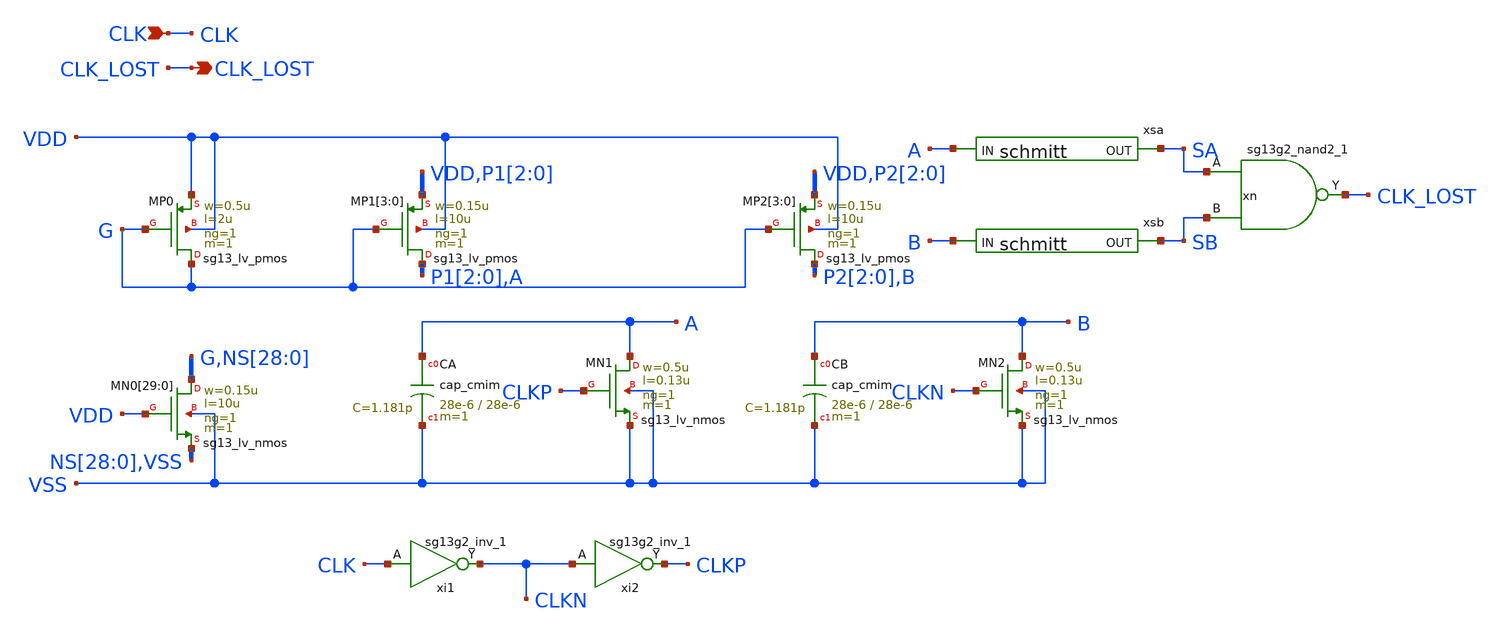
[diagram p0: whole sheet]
** sch_path: design/blocks/clkmon/schematic/wd_clkmon.sch
**.subckt wd_clkmon CLK CLK_LOST
*.ipin CLK
*.opin CLK_LOST
XMP0 G G VDD VDD sg13_lv_pmos w=0.5u l=2u ng=1 m=1 mm_ok=1
XMN0[29] G VDD NS[28] VSS sg13_lv_nmos w=0.15u l=10u ng=1 m=1 mm_ok=1
XMN0[28] NS[28] VDD NS[27] VSS sg13_lv_nmos w=0.15u l=10u ng=1 m=1 mm_ok=1
XMN0[27] NS[27] VDD NS[26] VSS sg13_lv_nmos w=0.15u l=10u ng=1 m=1 mm_ok=1
XMN0[26] NS[26] VDD NS[25] VSS sg13_lv_nmos w=0.15u l=10u ng=1 m=1 mm_ok=1
XMN0[25] NS[25] VDD NS[24] VSS sg13_lv_nmos w=0.15u l=10u ng=1 m=1 mm_ok=1
XMN0[24] NS[24] VDD NS[23] VSS sg13_lv_nmos w=0.15u l=10u ng=1 m=1 mm_ok=1
XMN0[23] NS[23] VDD NS[22] VSS sg13_lv_nmos w=0.15u l=10u ng=1 m=1 mm_ok=1
XMN0[22] NS[22] VDD NS[21] VSS sg13_lv_nmos w=0.15u l=10u ng=1 m=1 mm_ok=1
XMN0[21] NS[21] VDD NS[20] VSS sg13_lv_nmos w=0.15u l=10u ng=1 m=1 mm_ok=1
XMN0[20] NS[20] VDD NS[19] VSS sg13_lv_nmos w=0.15u l=10u ng=1 m=1 mm_ok=1
XMN0[19] NS[19] VDD NS[18] VSS sg13_lv_nmos w=0.15u l=10u ng=1 m=1 mm_ok=1
XMN0[18] NS[18] VDD NS[17] VSS sg13_lv_nmos w=0.15u l=10u ng=1 m=1 mm_ok=1
XMN0[17] NS[17] VDD NS[16] VSS sg13_lv_nmos w=0.15u l=10u ng=1 m=1 mm_ok=1
XMN0[16] NS[16] VDD NS[15] VSS sg13_lv_nmos w=0.15u l=10u ng=1 m=1 mm_ok=1
XMN0[15] NS[15] VDD NS[14] VSS sg13_lv_nmos w=0.15u l=10u ng=1 m=1 mm_ok=1
XMN0[14] NS[14] VDD NS[13] VSS sg13_lv_nmos w=0.15u l=10u ng=1 m=1 mm_ok=1
XMN0[13] NS[13] VDD NS[12] VSS sg13_lv_nmos w=0.15u l=10u ng=1 m=1 mm_ok=1
XMN0[12] NS[12] VDD NS[11] VSS sg13_lv_nmos w=0.15u l=10u ng=1 m=1 mm_ok=1
XMN0[11] NS[11] VDD NS[10] VSS sg13_lv_nmos w=0.15u l=10u ng=1 m=1 mm_ok=1
XMN0[10] NS[10] VDD NS[9] VSS sg13_lv_nmos w=0.15u l=10u ng=1 m=1 mm_ok=1
XMN0[9] NS[9] VDD NS[8] VSS sg13_lv_nmos w=0.15u l=10u ng=1 m=1 mm_ok=1
XMN0[8] NS[8] VDD NS[7] VSS sg13_lv_nmos w=0.15u l=10u ng=1 m=1 mm_ok=1
XMN0[7] NS[7] VDD NS[6] VSS sg13_lv_nmos w=0.15u l=10u ng=1 m=1 mm_ok=1
XMN0[6] NS[6] VDD NS[5] VSS sg13_lv_nmos w=0.15u l=10u ng=1 m=1 mm_ok=1
XMN0[5] NS[5] VDD NS[4] VSS sg13_lv_nmos w=0.15u l=10u ng=1 m=1 mm_ok=1
XMN0[4] NS[4] VDD NS[3] VSS sg13_lv_nmos w=0.15u l=10u ng=1 m=1 mm_ok=1
XMN0[3] NS[3] VDD NS[2] VSS sg13_lv_nmos w=0.15u l=10u ng=1 m=1 mm_ok=1
XMN0[2] NS[2] VDD NS[1] VSS sg13_lv_nmos w=0.15u l=10u ng=1 m=1 mm_ok=1
XMN0[1] NS[1] VDD NS[0] VSS sg13_lv_nmos w=0.15u l=10u ng=1 m=1 mm_ok=1
XMN0[0] NS[0] VDD VSS VSS sg13_lv_nmos w=0.15u l=10u ng=1 m=1 mm_ok=1
XMP1[3] P1[2] G VDD VDD sg13_lv_pmos w=0.15u l=10u ng=1 m=1 mm_ok=1
XMP1[2] P1[1] G P1[2] VDD sg13_lv_pmos w=0.15u l=10u ng=1 m=1 mm_ok=1
XMP1[1] P1[0] G P1[1] VDD sg13_lv_pmos w=0.15u l=10u ng=1 m=1 mm_ok=1
XMP1[0] A G P1[0] VDD sg13_lv_pmos w=0.15u l=10u ng=1 m=1 mm_ok=1
XCA A VSS cap_cmim w=28e-6 l=28e-6 m=1 mm_ok=1
XMN1 A CLKP VSS VSS sg13_lv_nmos w=0.5u l=0.13u ng=1 m=1 mm_ok=1
XMP2[3] P2[2] G VDD VDD sg13_lv_pmos w=0.15u l=10u ng=1 m=1 mm_ok=1
XMP2[2] P2[1] G P2[2] VDD sg13_lv_pmos w=0.15u l=10u ng=1 m=1 mm_ok=1
XMP2[1] P2[0] G P2[1] VDD sg13_lv_pmos w=0.15u l=10u ng=1 m=1 mm_ok=1
XMP2[0] B G P2[0] VDD sg13_lv_pmos w=0.15u l=10u ng=1 m=1 mm_ok=1
XCB B VSS cap_cmim w=28e-6 l=28e-6 m=1 mm_ok=1
XMN2 B CLKN VSS VSS sg13_lv_nmos w=0.5u l=0.13u ng=1 m=1 mm_ok=1
xi1 CLKN CLK VDD VSS sg13g2_inv_1
xi2 CLKP CLKN VDD VSS sg13g2_inv_1
xsa A SA VDD VSS schmitt
xsb B SB VDD VSS schmitt
xn CLK_LOST SA SB VDD VSS sg13g2_nand2_1
**.ends

* expanding   symbol:  sg13g2_inv_1.sym # of pins=2
** sym_path: sg13g2_inv_1.sym
** sch_path: sg13g2_inv_1.sch
.subckt sg13g2_inv_1 Y A VDD VSS
*.opin Y
*.ipin A
*.iopin VDD
*.iopin VSS
XM1 Y A VSS VSS sg13_lv_nmos w=740.00n l=130.00n ng=1 m=1 mm_ok=1
XM2 Y A VDD VDD sg13_lv_pmos w=1.12u l=130.00n ng=1 m=1 mm_ok=1
.ends


* expanding   symbol:  schmitt.sym # of pins=2
** sym_path: design/blocks/schmitt/schematic/schmitt.sym
** sch_path: design/blocks/schmitt/schematic/schmitt.sch
.subckt schmitt IN OUT VDD VSS
*.opin OUT
*.ipin IN
XM4 net1 IN VDD VDD sg13_lv_pmos w=1.04u l=0.13u ng=1 m=1 mm_ok=1
XM6 OUT IN net2 VSS sg13_lv_nmos w=0.76u l=0.13u ng=1 m=1 mm_ok=1
XM5 OUT IN net1 VDD sg13_lv_pmos w=1.04u l=0.13u ng=1 m=1 mm_ok=1
XM7 net2 IN VSS VSS sg13_lv_nmos w=0.76u l=0.13u ng=1 m=1 mm_ok=1
XM8 VSS OUT net1 VDD sg13_lv_pmos w=0.42u l=0.13u ng=1 m=1 mm_ok=1
XM9 VDD OUT net2 VSS sg13_lv_nmos w=0.42u l=0.13u ng=1 m=1 mm_ok=1
.ends


* expanding   symbol:  sg13g2_nand2_1.sym # of pins=3
** sym_path: sg13g2_nand2_1.sym
** sch_path: sg13g2_nand2_1.sch
.subckt sg13g2_nand2_1 Y A B VDD VSS
*.iopin VDD
*.iopin VSS
*.ipin A
*.ipin B
*.opin Y
XM1 Y A net1 VSS sg13_lv_nmos w=740.00n l=130.00n ng=1 m=1 mm_ok=1
XM2 net1 B VSS VSS sg13_lv_nmos w=740.00n l=130.00n ng=1 m=1 mm_ok=1
XM3 Y A VDD VDD sg13_lv_pmos w=1.12u l=130.00n ng=1 m=1 mm_ok=1
XM4 Y B VDD VDD sg13_lv_pmos w=1.12u l=130.00n ng=1 m=1 mm_ok=1
.ends

.end
